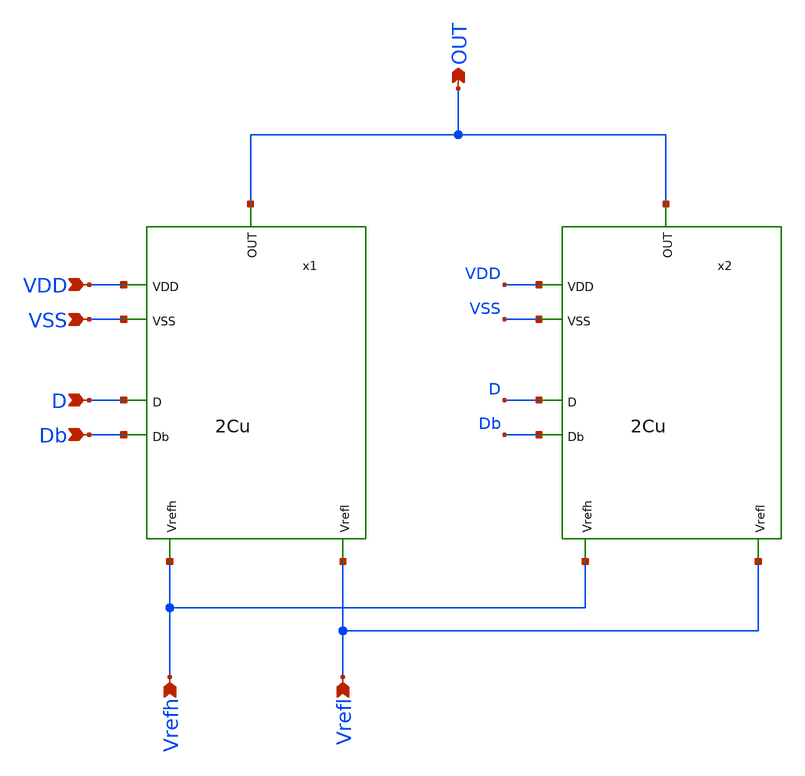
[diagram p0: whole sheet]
** sch_path: 4Cu.sch
**.subckt 4Cu OUT VDD D VSS Vrefh Vrefl Db
*.opin OUT
*.ipin VDD
*.ipin D
*.ipin VSS
*.ipin Vrefh
*.ipin Vrefl
*.ipin Db
x1 OUT VSS VDD Db D Vrefl Vrefh 2Cu
x2 OUT VSS VDD Db D Vrefl Vrefh 2Cu
**.ends
.end
